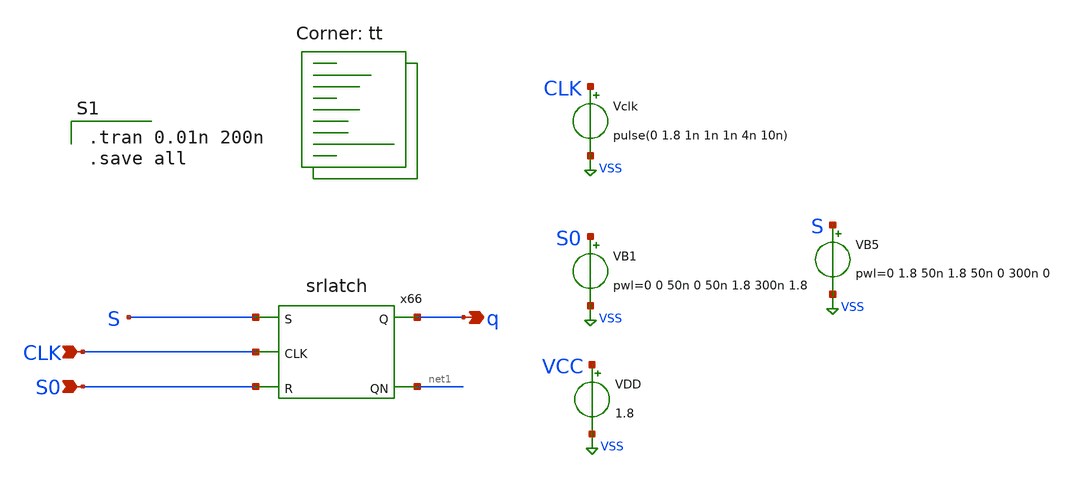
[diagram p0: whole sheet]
** sch_path: gates/srsim.sch
* StefanSchippers/xschem_sky130/sky130_tests/lvnand.sch:
* Copyright 2021 Stefan Frederik Schippers
* Licensed under the Apache License, Version 2.0 (the "License");
**.subckt srsim CLK S0 q
*.ipin CLK
*.ipin S0
*.opin q
x66 S CLK S0 q net1 srlatch
VDD VCC VSS 1.8
VB1 S0 VSS pwl=0 0 50n 0 50n 1.8 300n 1.8
Vclk CLK VSS pulse(0 1.8 1n 1n 1n 4n 10n)
VB5 S VSS pwl=0 1.8 50n 1.8 50n 0 300n 0
**** begin user architecture code

.tran 0.01n 200n
.save all

.lib $::SKYWATER_MODELS/sky130.lib.spice tt
**** end user architecture code
**.ends

* expanding   symbol:  sky130_tests/srlatch.sym # of pins=5
** sym_path: sky130_tests/srlatch.sym
** sch_path: sky130_tests/srlatch.sch
.subckt srlatch S CLK R Q QN
*.ipin S
*.ipin R
*.opin Q
*.opin QN
*.ipin CLK
x5 S CLK SN VCC VSS lvnand WidthN=1 LenN=0.15 WidthP=1 LenP=0.15 m=1
x1 R CLK RN VCC VSS lvnand WidthN=1 LenN=0.15 WidthP=1 LenP=0.15 m=1
x2 RN Q QN VCC VSS lvnand WidthN=1 LenN=0.15 WidthP=1 LenP=0.15 m=1
x3 SN QN Q VCC VSS lvnand WidthN=1 LenN=0.15 WidthP=1 LenP=0.15 m=1
.ends


* expanding   symbol:  sky130_tests/lvnand.sym # of pins=3
** sym_path: sky130_tests/lvnand.sym
** sch_path: sky130_tests/lvnand.sch
.subckt lvnand A B Y VCCPIN VSSPIN  WidthN=1 LenN=0.15 WidthP=1 LenP=0.15
*.ipin A
*.ipin B
*.opin Y
XM1 Y B S VSSPIN sky130_fd_pr__nfet_01v8 L=LenN W=WidthN nf=1 ad='int((nf+1)/2) * W/nf * 0.29' as='int((nf+2)/2) * W/nf * 0.29'
+ pd='2*int((nf+1)/2) * (W/nf + 0.29)' ps='2*int((nf+2)/2) * (W/nf + 0.29)' nrd='0.29 / W' nrs='0.29 / W'
+ sa=0 sb=0 sd=0 mult=1 m=1
XM2 Y A VCCPIN VCCPIN sky130_fd_pr__pfet_01v8 L=LenP W=WidthP nf=1 ad='int((nf+1)/2) * W/nf * 0.29' as='int((nf+2)/2) * W/nf * 0.29'
+ pd='2*int((nf+1)/2) * (W/nf + 0.29)' ps='2*int((nf+2)/2) * (W/nf + 0.29)' nrd='0.29 / W' nrs='0.29 / W'
+ sa=0 sb=0 sd=0 mult=1 m=1
XM3 Y B VCCPIN VCCPIN sky130_fd_pr__pfet_01v8 L=LenP W=WidthP nf=1 ad='int((nf+1)/2) * W/nf * 0.29' as='int((nf+2)/2) * W/nf * 0.29'
+ pd='2*int((nf+1)/2) * (W/nf + 0.29)' ps='2*int((nf+2)/2) * (W/nf + 0.29)' nrd='0.29 / W' nrs='0.29 / W'
+ sa=0 sb=0 sd=0 mult=1 m=1
XM4 S A VSSPIN VSSPIN sky130_fd_pr__nfet_01v8 L=LenN W=WidthN nf=1 ad='int((nf+1)/2) * W/nf * 0.29' as='int((nf+2)/2) * W/nf * 0.29'
+ pd='2*int((nf+1)/2) * (W/nf + 0.29)' ps='2*int((nf+2)/2) * (W/nf + 0.29)' nrd='0.29 / W' nrs='0.29 / W'
+ sa=0 sb=0 sd=0 mult=1 m=1
.ends

.GLOBAL VSS
.end
